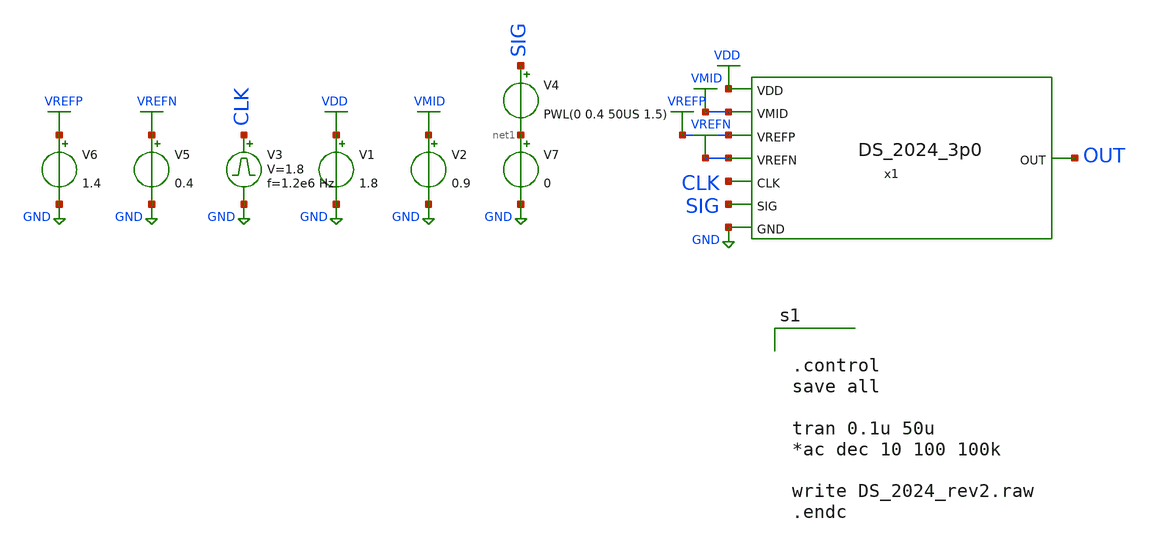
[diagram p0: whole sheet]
** sch_path: DeltaSigma/xschem/DS_2024_Bench.sch
.lib $::SKYWATER_MODELS/sky130.lib.spice tt
.include $::SKYWATER_STDCELLS/sky130_fd_sc_hd.spice

**.subckt DS_2024_Bench
V1 VDD GND 1.8
V2 VMID GND 0.9
V3 CLK GND pulse 0 1.8 '0.495/ 1.2e6 ' '0.01/1.2e6 ' '0.01/1.2e6 ' '0.49/1.2e6 ' '1/1.2e6 '
V5 VREFN GND 0.4
V6 VREFP GND 1.4
x1 VDD VMID OUT VREFP VREFN GND SIG CLK DS_2024_3p0
V4 SIG net1 PWL(0 0.4 50US 1.5)
V7 net1 GND 0
**** begin user architecture code


.control
save all

tran 0.1u 50u
*ac dec 10 100 100k

write DS_2024_rev2.raw
.endc


**** end user architecture code
**.ends
.GLOBAL VDD
.GLOBAL GND
.GLOBAL VMID
.GLOBAL VREFN
.GLOBAL VREFP
.end
